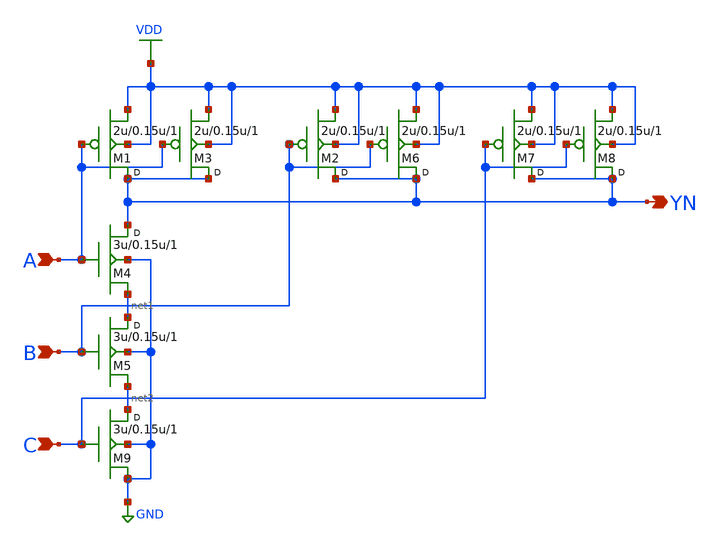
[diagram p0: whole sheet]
** sch_path: lib/xschem/schematics/NAND3X2.sch
**.subckt NAND3X2 A B YN C
*.ipin A
*.ipin B
*.opin YN
*.ipin C
M1 YN A VDD VDD pmos w=2u l=0.15u m=1
M2 YN B VDD VDD pmos w=2u l=0.15u m=1
M4 YN A net1 GND nmos w=3u l=0.15u m=1
M5 net1 B net2 GND nmos w=3u l=0.15u m=1
M3 YN A VDD VDD pmos w=2u l=0.15u m=1
M6 YN B VDD VDD pmos w=2u l=0.15u m=1
M7 YN C VDD VDD pmos w=2u l=0.15u m=1
M8 YN C VDD VDD pmos w=2u l=0.15u m=1
M9 net2 C GND GND nmos w=3u l=0.15u m=1
**.ends
.GLOBAL GND
.GLOBAL VDD
.end
